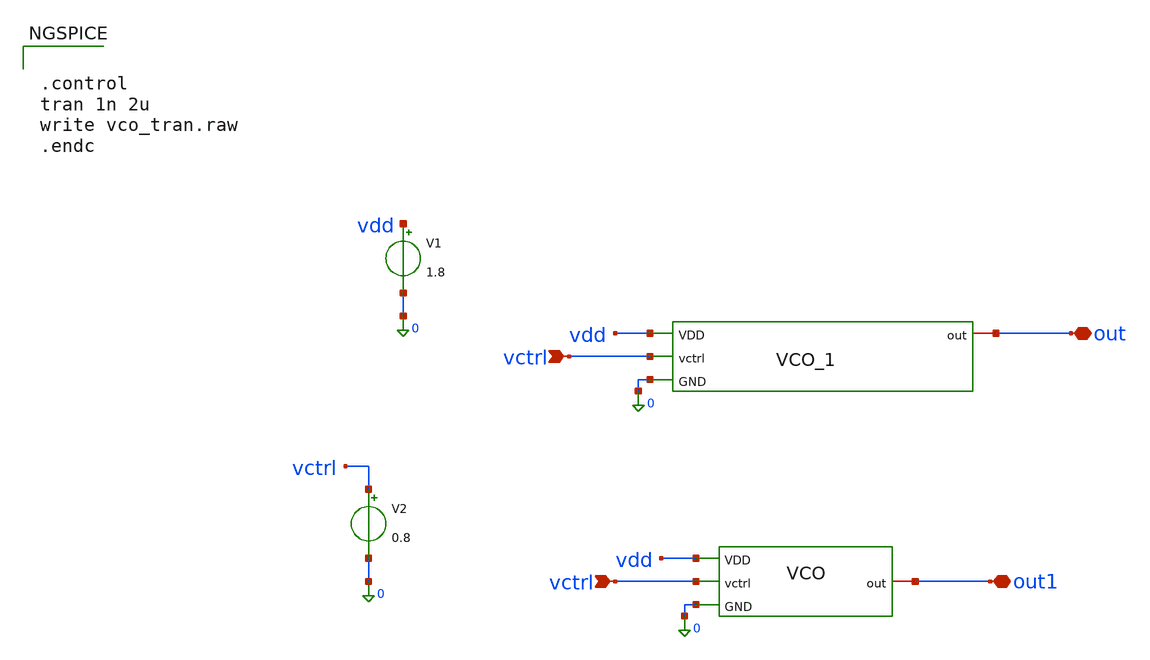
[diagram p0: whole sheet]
** sch_path: design_data/xschem/VCO/vco_tran.sch
**.subckt vco_tran vctrl out vctrl out1
*.ipin vctrl
*.iopin out
*.ipin vctrl
*.iopin out1
V1 vdd 0 1.8
V2 vctrl 0 0.8
x2 vdd out vctrl 0 vco_1
x1 vdd out1 vctrl 0 vco
**** begin user architecture code


.control
tran 1n 2u
write vco_tran.raw
.endc



** opencircuitdesign pdks install
.lib $::SKYWATER_MODELS/sky130.lib.spice tt

**** end user architecture code
**.ends

* expanding   symbol:  xschem/VCO/vco_1.sym # of pins=4
** sym_path: design_data/xschem/VCO/vco_1.sym
** sch_path: design_data/xschem/VCO/vco_1.sch
.subckt vco_1 VDD out vctrl GND
*.ipin vctrl
*.iopin out
*.ipin GND
*.ipin VDD
XM7 net4 net4 VDD VDD sky130_fd_pr__pfet_01v8 L=3.2 W=70 nf=1 ad='int((1 + 1)/2) * 70 / 1 * 0.29' as='int((1 + 2)/2) * 70 / 1 * 0.29'
+ pd='2*int((1 + 1)/2) * (70 / 1 + 0.29)' ps='2*int((1 + 2)/2) * (70 / 1 + 0.29)' nrd='0.29 / 70 ' nrs='0.29 / 70 '
+ sa=0 sb=0 sd=0 mult=1 m=1
XM8 net4 vctrl GND GND sky130_fd_pr__nfet_01v8 L=4.2 W=40 nf=1 ad='int((1 + 1)/2) * 40 / 1 * 0.29' as='int((1 + 2)/2) * 40 / 1 * 0.29'
+ pd='2*int((1 + 1)/2) * (40 / 1 + 0.29)' ps='2*int((1 + 2)/2) * (40 / 1 + 0.29)' nrd='0.29 / 40 ' nrs='0.29 / 40 '
+ sa=0 sb=0 sd=0 mult=1 m=1
XM5 net11 vctrl GND GND sky130_fd_pr__nfet_01v8 L=4.2 W=40 nf=1 ad='int((1 + 1)/2) * 40 / 1 * 0.29' as='int((1 + 2)/2) * 40 / 1 * 0.29'
+ pd='2*int((1 + 1)/2) * (40 / 1 + 0.29)' ps='2*int((1 + 2)/2) * (40 / 1 + 0.29)' nrd='0.29 / 40 ' nrs='0.29 / 40 '
+ sa=0 sb=0 sd=0 mult=1 m=1
XM6 net1 net3 net11 GND sky130_fd_pr__nfet_01v8 L=1.4 W=49 nf=1 ad='int((1 + 1)/2) * 49 / 1 * 0.29' as='int((1 + 2)/2) * 49 / 1 * 0.29'
+ pd='2*int((1 + 1)/2) * (49 / 1 + 0.29)' ps='2*int((1 + 2)/2) * (49 / 1 + 0.29)' nrd='0.29 / 49 ' nrs='0.29 / 49 '
+ sa=0 sb=0 sd=0 mult=1 m=1
XM1 net2 net4 VDD VDD sky130_fd_pr__pfet_01v8 L=3.2 W=70 nf=1 ad='int((1 + 1)/2) * 70 / 1 * 0.29' as='int((1 + 2)/2) * 70 / 1 * 0.29'
+ pd='2*int((1 + 1)/2) * (70 / 1 + 0.29)' ps='2*int((1 + 2)/2) * (70 / 1 + 0.29)' nrd='0.29 / 70 ' nrs='0.29 / 70 '
+ sa=0 sb=0 sd=0 mult=1 m=1
XM2 net1 net3 net2 net2 sky130_fd_pr__pfet_01v8 L=1.4 W=74 nf=1 ad='int((1 + 1)/2) * 74 / 1 * 0.29' as='int((1 + 2)/2) * 74 / 1 * 0.29'
+ pd='2*int((1 + 1)/2) * (74 / 1 + 0.29)' ps='2*int((1 + 2)/2) * (74 / 1 + 0.29)' nrd='0.29 / 74 ' nrs='0.29 / 74 '
+ sa=0 sb=0 sd=0 mult=1 m=1
XM3 net10 vctrl GND GND sky130_fd_pr__nfet_01v8 L=4.2 W=40 nf=1 ad='int((1 + 1)/2) * 40 / 1 * 0.29' as='int((1 + 2)/2) * 40 / 1 * 0.29'
+ pd='2*int((1 + 1)/2) * (40 / 1 + 0.29)' ps='2*int((1 + 2)/2) * (40 / 1 + 0.29)' nrd='0.29 / 40 ' nrs='0.29 / 40 '
+ sa=0 sb=0 sd=0 mult=1 m=1
XM9 net5 net4 VDD VDD sky130_fd_pr__pfet_01v8 L=3.2 W=70 nf=1 ad='int((1 + 1)/2) * 70 / 1 * 0.29' as='int((1 + 2)/2) * 70 / 1 * 0.29'
+ pd='2*int((1 + 1)/2) * (70 / 1 + 0.29)' ps='2*int((1 + 2)/2) * (70 / 1 + 0.29)' nrd='0.29 / 70 ' nrs='0.29 / 70 '
+ sa=0 sb=0 sd=0 mult=1 m=1
XM11 net9 vctrl GND GND sky130_fd_pr__nfet_01v8 L=4.2 W=40 nf=1 ad='int((1 + 1)/2) * 40 / 1 * 0.29' as='int((1 + 2)/2) * 40 / 1 * 0.29'
+ pd='2*int((1 + 1)/2) * (40 / 1 + 0.29)' ps='2*int((1 + 2)/2) * (40 / 1 + 0.29)' nrd='0.29 / 40 ' nrs='0.29 / 40 '
+ sa=0 sb=0 sd=0 mult=1 m=1
XM13 net6 net4 VDD VDD sky130_fd_pr__pfet_01v8 L=3.2 W=70 nf=1 ad='int((1 + 1)/2) * 70 / 1 * 0.29' as='int((1 + 2)/2) * 70 / 1 * 0.29'
+ pd='2*int((1 + 1)/2) * (70 / 1 + 0.29)' ps='2*int((1 + 2)/2) * (70 / 1 + 0.29)' nrd='0.29 / 70 ' nrs='0.29 / 70 '
+ sa=0 sb=0 sd=0 mult=1 m=1
XM4 net7 net1 net10 GND sky130_fd_pr__nfet_01v8 L=1.4 W=49 nf=1 ad='int((1 + 1)/2) * 49 / 1 * 0.29' as='int((1 + 2)/2) * 49 / 1 * 0.29'
+ pd='2*int((1 + 1)/2) * (49 / 1 + 0.29)' ps='2*int((1 + 2)/2) * (49 / 1 + 0.29)' nrd='0.29 / 49 ' nrs='0.29 / 49 '
+ sa=0 sb=0 sd=0 mult=1 m=1
XM10 net7 net1 net5 net5 sky130_fd_pr__pfet_01v8 L=1.4 W=74 nf=1 ad='int((1 + 1)/2) * 74 / 1 * 0.29'
+ as='int((1 + 2)/2) * 74 / 1 * 0.29' pd='2*int((1 + 1)/2) * (74 / 1 + 0.29)' ps='2*int((1 + 2)/2) * (74 / 1 + 0.29)'
+ nrd='0.29 / 74 ' nrs='0.29 / 74 ' sa=0 sb=0 sd=0 mult=1 m=1
XM12 net3 net7 net9 GND sky130_fd_pr__nfet_01v8 L=1.4 W=49 nf=1 ad='int((1 + 1)/2) * 49 / 1 * 0.29' as='int((1 + 2)/2) * 49 / 1 * 0.29'
+ pd='2*int((1 + 1)/2) * (49 / 1 + 0.29)' ps='2*int((1 + 2)/2) * (49 / 1 + 0.29)' nrd='0.29 / 49 ' nrs='0.29 / 49 '
+ sa=0 sb=0 sd=0 mult=1 m=1
XM14 net3 net7 net6 net6 sky130_fd_pr__pfet_01v8 L=1.4 W=74 nf=1 ad='int((1 + 1)/2) * 74 / 1 * 0.29'
+ as='int((1 + 2)/2) * 74 / 1 * 0.29' pd='2*int((1 + 1)/2) * (74 / 1 + 0.29)' ps='2*int((1 + 2)/2) * (74 / 1 + 0.29)'
+ nrd='0.29 / 74 ' nrs='0.29 / 74 ' sa=0 sb=0 sd=0 mult=1 m=1
XM15 net8 net3 GND GND sky130_fd_pr__nfet_01v8 L=1 W=10 nf=1 ad='int((1 + 1)/2) * 10 / 1 * 0.29' as='int((1 + 2)/2) * 10 / 1 * 0.29'
+ pd='2*int((1 + 1)/2) * (10 / 1 + 0.29)' ps='2*int((1 + 2)/2) * (10 / 1 + 0.29)' nrd='0.29 / 10 ' nrs='0.29 / 10 '
+ sa=0 sb=0 sd=0 mult=1 m=1
XM16 net8 net3 VDD VDD sky130_fd_pr__pfet_01v8 L=1 W=20 nf=1 ad='int((1 + 1)/2) * 20 / 1 * 0.29' as='int((1 + 2)/2) * 20 / 1 * 0.29'
+ pd='2*int((1 + 1)/2) * (20 / 1 + 0.29)' ps='2*int((1 + 2)/2) * (20 / 1 + 0.29)' nrd='0.29 / 20 ' nrs='0.29 / 20 '
+ sa=0 sb=0 sd=0 mult=1 m=1
XM17 out net8 GND GND sky130_fd_pr__nfet_01v8 L=1 W=20 nf=1 ad='int((1 + 1)/2) * 20 / 1 * 0.29' as='int((1 + 2)/2) * 20 / 1 * 0.29'
+ pd='2*int((1 + 1)/2) * (20 / 1 + 0.29)' ps='2*int((1 + 2)/2) * (20 / 1 + 0.29)' nrd='0.29 / 20 ' nrs='0.29 / 20 '
+ sa=0 sb=0 sd=0 mult=1 m=1
XM18 out net8 VDD VDD sky130_fd_pr__pfet_01v8 L=1 W=40 nf=1 ad='int((1 + 1)/2) * 40 / 1 * 0.29' as='int((1 + 2)/2) * 40 / 1 * 0.29'
+ pd='2*int((1 + 1)/2) * (40 / 1 + 0.29)' ps='2*int((1 + 2)/2) * (40 / 1 + 0.29)' nrd='0.29 / 40 ' nrs='0.29 / 40 '
+ sa=0 sb=0 sd=0 mult=1 m=1
.ends


* expanding   symbol:  xschem/VCO/vco.sym # of pins=4
** sym_path: design_data/xschem/VCO/vco.sym
** sch_path: design_data/xschem/VCO/vco.sch
.subckt vco VDD out vctrl GND
*.ipin vctrl
*.iopin out
*.ipin GND
*.ipin VDD
XM7 net4 net4 VDD VDD sky130_fd_pr__pfet_01v8 L=3.2 W=70 nf=1 ad='int((1 + 1)/2) * 70 / 1 * 0.29' as='int((1 + 2)/2) * 70 / 1 * 0.29'
+ pd='2*int((1 + 1)/2) * (70 / 1 + 0.29)' ps='2*int((1 + 2)/2) * (70 / 1 + 0.29)' nrd='0.29 / 70 ' nrs='0.29 / 70 '
+ sa=0 sb=0 sd=0 mult=1 m=1
XM8 net4 vctrl GND GND sky130_fd_pr__nfet_01v8 L=4.2 W=40 nf=1 ad='int((1 + 1)/2) * 40 / 1 * 0.29' as='int((1 + 2)/2) * 40 / 1 * 0.29'
+ pd='2*int((1 + 1)/2) * (40 / 1 + 0.29)' ps='2*int((1 + 2)/2) * (40 / 1 + 0.29)' nrd='0.29 / 40 ' nrs='0.29 / 40 '
+ sa=0 sb=0 sd=0 mult=1 m=1
XM5 net11 vctrl GND GND sky130_fd_pr__nfet_01v8 L=4.2 W=40 nf=1 ad='int((1 + 1)/2) * 40 / 1 * 0.29' as='int((1 + 2)/2) * 40 / 1 * 0.29'
+ pd='2*int((1 + 1)/2) * (40 / 1 + 0.29)' ps='2*int((1 + 2)/2) * (40 / 1 + 0.29)' nrd='0.29 / 40 ' nrs='0.29 / 40 '
+ sa=0 sb=0 sd=0 mult=1 m=1
XM6 net1 net3 net11 GND sky130_fd_pr__nfet_01v8 L=1.4 W=49 nf=1 ad='int((1 + 1)/2) * 49 / 1 * 0.29' as='int((1 + 2)/2) * 49 / 1 * 0.29'
+ pd='2*int((1 + 1)/2) * (49 / 1 + 0.29)' ps='2*int((1 + 2)/2) * (49 / 1 + 0.29)' nrd='0.29 / 49 ' nrs='0.29 / 49 '
+ sa=0 sb=0 sd=0 mult=1 m=1
XM1 net2 net4 VDD VDD sky130_fd_pr__pfet_01v8 L=3.2 W=70 nf=1 ad='int((1 + 1)/2) * 70 / 1 * 0.29' as='int((1 + 2)/2) * 70 / 1 * 0.29'
+ pd='2*int((1 + 1)/2) * (70 / 1 + 0.29)' ps='2*int((1 + 2)/2) * (70 / 1 + 0.29)' nrd='0.29 / 70 ' nrs='0.29 / 70 '
+ sa=0 sb=0 sd=0 mult=1 m=1
XM2 net1 net3 net2 net2 sky130_fd_pr__pfet_01v8 L=1.4 W=74 nf=1 ad='int((1 + 1)/2) * 74 / 1 * 0.29' as='int((1 + 2)/2) * 74 / 1 * 0.29'
+ pd='2*int((1 + 1)/2) * (74 / 1 + 0.29)' ps='2*int((1 + 2)/2) * (74 / 1 + 0.29)' nrd='0.29 / 74 ' nrs='0.29 / 74 '
+ sa=0 sb=0 sd=0 mult=1 m=1
XM3 net10 vctrl GND GND sky130_fd_pr__nfet_01v8 L=4.2 W=40 nf=1 ad='int((1 + 1)/2) * 40 / 1 * 0.29' as='int((1 + 2)/2) * 40 / 1 * 0.29'
+ pd='2*int((1 + 1)/2) * (40 / 1 + 0.29)' ps='2*int((1 + 2)/2) * (40 / 1 + 0.29)' nrd='0.29 / 40 ' nrs='0.29 / 40 '
+ sa=0 sb=0 sd=0 mult=1 m=1
XM9 net5 net4 VDD VDD sky130_fd_pr__pfet_01v8 L=3.2 W=70 nf=1 ad='int((1 + 1)/2) * 70 / 1 * 0.29' as='int((1 + 2)/2) * 70 / 1 * 0.29'
+ pd='2*int((1 + 1)/2) * (70 / 1 + 0.29)' ps='2*int((1 + 2)/2) * (70 / 1 + 0.29)' nrd='0.29 / 70 ' nrs='0.29 / 70 '
+ sa=0 sb=0 sd=0 mult=1 m=1
XM11 net9 vctrl GND GND sky130_fd_pr__nfet_01v8 L=4.2 W=40 nf=1 ad='int((1 + 1)/2) * 40 / 1 * 0.29' as='int((1 + 2)/2) * 40 / 1 * 0.29'
+ pd='2*int((1 + 1)/2) * (40 / 1 + 0.29)' ps='2*int((1 + 2)/2) * (40 / 1 + 0.29)' nrd='0.29 / 40 ' nrs='0.29 / 40 '
+ sa=0 sb=0 sd=0 mult=1 m=1
XM13 net6 net4 VDD VDD sky130_fd_pr__pfet_01v8 L=3.2 W=70 nf=1 ad='int((1 + 1)/2) * 70 / 1 * 0.29' as='int((1 + 2)/2) * 70 / 1 * 0.29'
+ pd='2*int((1 + 1)/2) * (70 / 1 + 0.29)' ps='2*int((1 + 2)/2) * (70 / 1 + 0.29)' nrd='0.29 / 70 ' nrs='0.29 / 70 '
+ sa=0 sb=0 sd=0 mult=1 m=1
XM4 net7 net1 net10 GND sky130_fd_pr__nfet_01v8 L=1.4 W=49 nf=1 ad='int((1 + 1)/2) * 49 / 1 * 0.29' as='int((1 + 2)/2) * 49 / 1 * 0.29'
+ pd='2*int((1 + 1)/2) * (49 / 1 + 0.29)' ps='2*int((1 + 2)/2) * (49 / 1 + 0.29)' nrd='0.29 / 49 ' nrs='0.29 / 49 '
+ sa=0 sb=0 sd=0 mult=1 m=1
XM10 net7 net1 net5 net5 sky130_fd_pr__pfet_01v8 L=1.4 W=74 nf=1 ad='int((1 + 1)/2) * 74 / 1 * 0.29'
+ as='int((1 + 2)/2) * 74 / 1 * 0.29' pd='2*int((1 + 1)/2) * (74 / 1 + 0.29)' ps='2*int((1 + 2)/2) * (74 / 1 + 0.29)'
+ nrd='0.29 / 74 ' nrs='0.29 / 74 ' sa=0 sb=0 sd=0 mult=1 m=1
XM12 net3 net7 net9 GND sky130_fd_pr__nfet_01v8 L=1.4 W=49 nf=1 ad='int((1 + 1)/2) * 49 / 1 * 0.29' as='int((1 + 2)/2) * 49 / 1 * 0.29'
+ pd='2*int((1 + 1)/2) * (49 / 1 + 0.29)' ps='2*int((1 + 2)/2) * (49 / 1 + 0.29)' nrd='0.29 / 49 ' nrs='0.29 / 49 '
+ sa=0 sb=0 sd=0 mult=1 m=1
XM14 net3 net7 net6 net6 sky130_fd_pr__pfet_01v8 L=1.4 W=74 nf=1 ad='int((1 + 1)/2) * 74 / 1 * 0.29'
+ as='int((1 + 2)/2) * 74 / 1 * 0.29' pd='2*int((1 + 1)/2) * (74 / 1 + 0.29)' ps='2*int((1 + 2)/2) * (74 / 1 + 0.29)'
+ nrd='0.29 / 74 ' nrs='0.29 / 74 ' sa=0 sb=0 sd=0 mult=1 m=1
XM15 net8 net3 GND GND sky130_fd_pr__nfet_01v8 L=1 W=10 nf=1 ad='int((1 + 1)/2) * 10 / 1 * 0.29' as='int((1 + 2)/2) * 10 / 1 * 0.29'
+ pd='2*int((1 + 1)/2) * (10 / 1 + 0.29)' ps='2*int((1 + 2)/2) * (10 / 1 + 0.29)' nrd='0.29 / 10 ' nrs='0.29 / 10 '
+ sa=0 sb=0 sd=0 mult=1 m=1
XM16 net8 net3 VDD VDD sky130_fd_pr__pfet_01v8 L=1 W=20 nf=1 ad='int((1 + 1)/2) * 20 / 1 * 0.29' as='int((1 + 2)/2) * 20 / 1 * 0.29'
+ pd='2*int((1 + 1)/2) * (20 / 1 + 0.29)' ps='2*int((1 + 2)/2) * (20 / 1 + 0.29)' nrd='0.29 / 20 ' nrs='0.29 / 20 '
+ sa=0 sb=0 sd=0 mult=1 m=1
XM17 out net8 GND GND sky130_fd_pr__nfet_01v8 L=1 W=20 nf=1 ad='int((1 + 1)/2) * 20 / 1 * 0.29' as='int((1 + 2)/2) * 20 / 1 * 0.29'
+ pd='2*int((1 + 1)/2) * (20 / 1 + 0.29)' ps='2*int((1 + 2)/2) * (20 / 1 + 0.29)' nrd='0.29 / 20 ' nrs='0.29 / 20 '
+ sa=0 sb=0 sd=0 mult=1 m=1
XM18 out net8 VDD VDD sky130_fd_pr__pfet_01v8 L=1 W=40 nf=1 ad='int((1 + 1)/2) * 40 / 1 * 0.29' as='int((1 + 2)/2) * 40 / 1 * 0.29'
+ pd='2*int((1 + 1)/2) * (40 / 1 + 0.29)' ps='2*int((1 + 2)/2) * (40 / 1 + 0.29)' nrd='0.29 / 40 ' nrs='0.29 / 40 '
+ sa=0 sb=0 sd=0 mult=1 m=1
.ends

.end
